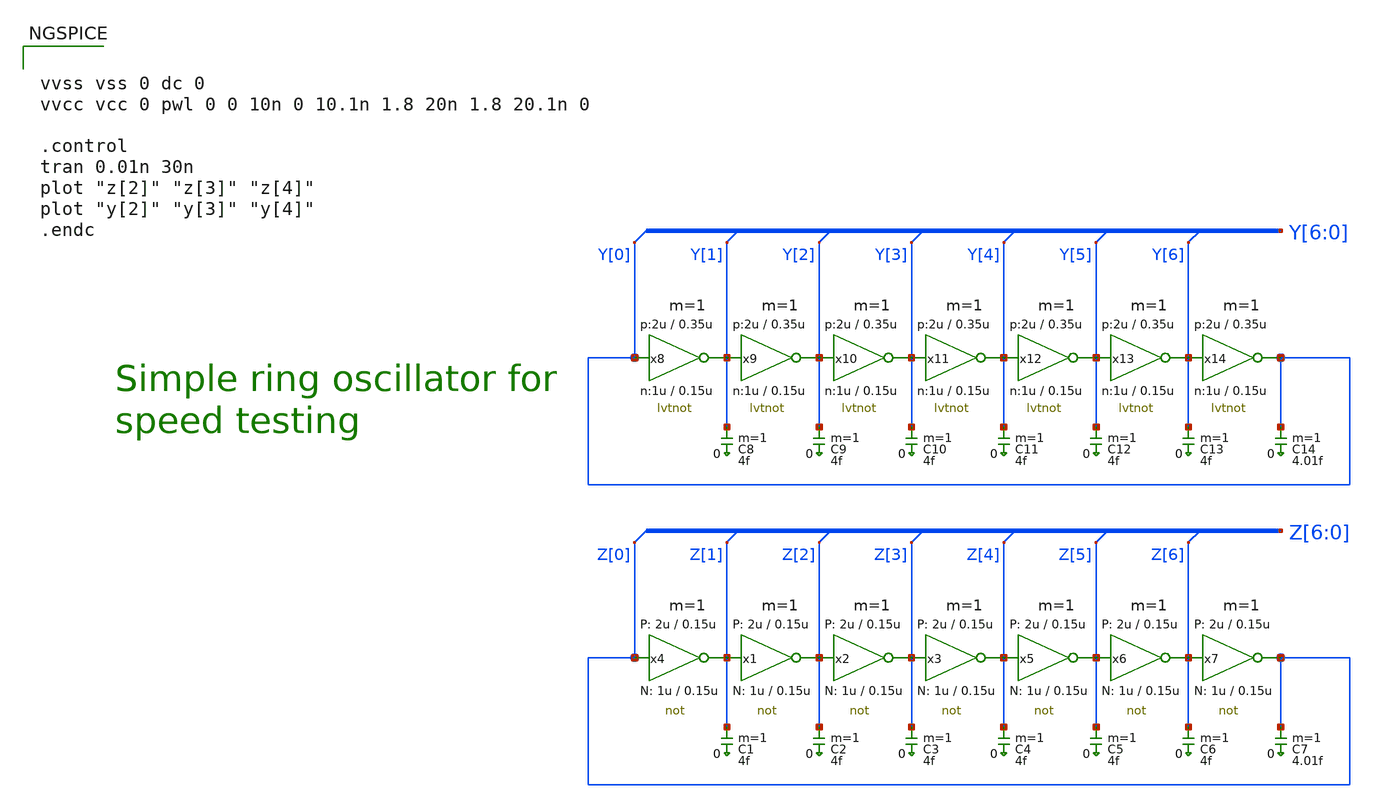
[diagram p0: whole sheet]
** sch_path: sky130_tests_ng/test_inv.sch
* Copyright 2020 Stefan Frederik Schippers
* Licensed under the Apache License, Version 2.0 (the "License");
* you may not use this file except in compliance with the License.
* You may obtain a copy of the License at
* https://www.apache.org/licenses/LICENSE-2.0
* Unless required by applicable law or agreed to in writing, software
* distributed under the License is distributed on an "AS IS" BASIS,
* WITHOUT WARRANTIES OR CONDITIONS OF ANY KIND, either express or implied.
* See the License for the specific language governing permissions and
* limitations under the License.
* StefanSchippers/xschem_sky130/sky130_tests/not.sch:
* Copyright 2021 Stefan Frederik Schippers
**.subckt test_inv
C1 Z[1] 0 4f m=1
C2 Z[2] 0 4f m=1
C3 Z[3] 0 4f m=1
C4 Z[4] 0 4f m=1
C5 Z[5] 0 4f m=1
C6 Z[6] 0 4f m=1
C7 Z[0] 0 4.01f m=1
C8 Y[1] 0 4f m=1
C9 Y[2] 0 4f m=1
C10 Y[3] 0 4f m=1
C11 Y[4] 0 4f m=1
C12 Y[5] 0 4f m=1
C13 Y[6] 0 4f m=1
C14 Y[0] 0 4.01f m=1
x4 Z[1] Z[0] VCC VSS not W_N=1u L_N=0.15u W_P=2u L_P=0.15u m=1
x1 Z[2] Z[1] VCC VSS not W_N=1u L_N=0.15u W_P=2u L_P=0.15u m=1
x2 Z[3] Z[2] VCC VSS not W_N=1u L_N=0.15u W_P=2u L_P=0.15u m=1
x3 Z[4] Z[3] VCC VSS not W_N=1u L_N=0.15u W_P=2u L_P=0.15u m=1
x5 Z[5] Z[4] VCC VSS not W_N=1u L_N=0.15u W_P=2u L_P=0.15u m=1
x6 Z[6] Z[5] VCC VSS not W_N=1u L_N=0.15u W_P=2u L_P=0.15u m=1
x7 Z[0] Z[6] VCC VSS not W_N=1u L_N=0.15u W_P=2u L_P=0.15u m=1
x8 Y[0] Y[1] VCC VSS lvtnot W_N=1u L_N=0.15u W_P=2u L_P=0.35u m=1
x9 Y[1] Y[2] VCC VSS lvtnot W_N=1u L_N=0.15u W_P=2u L_P=0.35u m=1
x10 Y[2] Y[3] VCC VSS lvtnot W_N=1u L_N=0.15u W_P=2u L_P=0.35u m=1
x11 Y[3] Y[4] VCC VSS lvtnot W_N=1u L_N=0.15u W_P=2u L_P=0.35u m=1
x12 Y[4] Y[5] VCC VSS lvtnot W_N=1u L_N=0.15u W_P=2u L_P=0.35u m=1
x13 Y[5] Y[6] VCC VSS lvtnot W_N=1u L_N=0.15u W_P=2u L_P=0.35u m=1
x14 Y[6] Y[0] VCC VSS lvtnot W_N=1u L_N=0.15u W_P=2u L_P=0.35u m=1
**** begin user architecture code


vvss vss 0 dc 0
vvcc vcc 0 pwl 0 0 10n 0 10.1n 1.8 20n 1.8 20.1n 0

.control
tran 0.01n 30n
plot "z[2]" "z[3]" "z[4]"
plot "y[2]" "y[3]" "y[4]"
.endc



**** end user architecture code
**.ends

* expanding   symbol:  sky130_tests/not.sym # of pins=2
** sym_path: sky130_tests/not.sym
** sch_path: sky130_tests/not.sch
.subckt not y a VCCPIN VSSPIN     W_N=1 L_N=0.15 W_P=2 L_P=0.15
*.opin y
*.ipin a
XM1 DN a VSSPIN VSSPIN sky130_fd_pr__nfet_01v8 w=W_N l=L_N ad=[sky130_fet_ad_cb W_N ]
+ pd=[sky130_fet_pd_cb W_N ] as=[sky130_fet_ad_cb W_N ] ps=[sky130_fet_pd_cb W_N ] nrd=[sky130_fet_nrd_cb W_N ]
+ nrs=[sky130_fet_nrd_cb W_N ] sa=0 sb=0 sd=0 nf=1 mult=1 m=1
XM2 DP a VCCPIN VCCPIN sky130_fd_pr__pfet_01v8 w=W_P l=L_P ad=[sky130_fet_ad_cb W_P ]
+ pd=[sky130_fet_pd_cb W_P ] as=[sky130_fet_ad_cb W_P ] ps=[sky130_fet_pd_cb W_P ] nrd=[sky130_fet_nrd_cb W_P ]
+ nrs=[sky130_fet_nrd_cb W_P ] sa=0 sb=0 sd=0 nf=1 mult=1 m=1
Vmeas DP y 0
.save i(vmeas)
Vmeas1 y DN 0
.save i(vmeas1)
.save v(dp)
.save v(dn)
.ends


* expanding   symbol:  sky130_tests/lvtnot.sym # of pins=2
** sym_path: sky130_tests/lvtnot.sym
** sch_path: sky130_tests/lvtnot.sch
.subckt lvtnot a y VCCPIN VSSPIN     W_N=1 L_N=0.15 W_P=2 L_P=0.35
*.opin y
*.ipin a
XM1 y a VSSPIN VSSPIN sky130_fd_pr__nfet_01v8_lvt w=W_N l=L_N ad=[sky130_fet_ad_cb W_N ]
+ pd=[sky130_fet_pd_cb W_N ] as=[sky130_fet_ad_cb W_N ] ps=[sky130_fet_pd_cb W_N ] nrd=[sky130_fet_nrd_cb W_N ]
+ nrs=[sky130_fet_nrd_cb W_N ] sa=0 sb=0 sd=0 nf=1 mult=1 m=1
XM2 y a VCCPIN VCCPIN sky130_fd_pr__pfet_01v8_lvt w=W_P l=L_P ad=[sky130_fet_ad_cb W_P ]
+ pd=[sky130_fet_pd_cb W_P ] as=[sky130_fet_ad_cb W_P ] ps=[sky130_fet_pd_cb W_P ] nrd=[sky130_fet_nrd_cb W_P ]
+ nrs=[sky130_fet_nrd_cb W_P ] sa=0 sb=0 sd=0 nf=1 mult=1 m=1
.ends

.end
